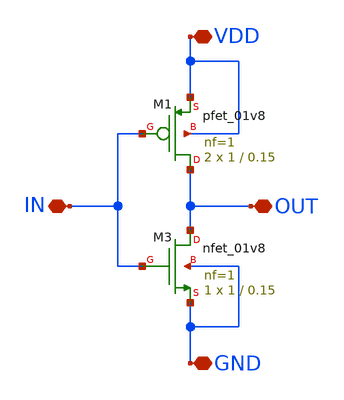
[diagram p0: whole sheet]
** sch_path: DIV/inv_DIV/inv_DIV.sch
**.subckt inv_DIV VDD OUT GND IN
*.iopin VDD
*.iopin OUT
*.iopin GND
*.iopin IN
XM3 OUT IN GND GND sky130_fd_pr__nfet_01v8 L=0.15 W=1 nf=1 ad='int((nf+1)/2) * W/nf * 0.29' as='int((nf+2)/2) * W/nf * 0.29'
+ pd='2*int((nf+1)/2) * (W/nf + 0.29)' ps='2*int((nf+2)/2) * (W/nf + 0.29)' nrd='0.29 / W' nrs='0.29 / W'
+ sa=0 sb=0 sd=0 mult=1 m=1
XM1 OUT IN VDD VDD sky130_fd_pr__pfet_01v8 L=0.15 W=1 nf=1 ad='int((nf+1)/2) * W/nf * 0.29' as='int((nf+2)/2) * W/nf * 0.29'
+ pd='2*int((nf+1)/2) * (W/nf + 0.29)' ps='2*int((nf+2)/2) * (W/nf + 0.29)' nrd='0.29 / W' nrs='0.29 / W'
+ sa=0 sb=0 sd=0 mult=2 m=2
**.ends
.end
